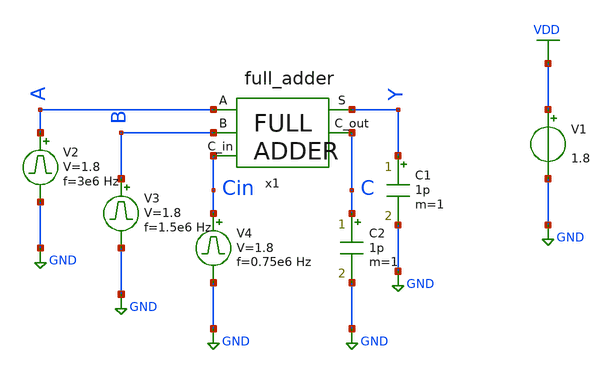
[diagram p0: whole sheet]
** sch_path: library/xschem/full_adder_tb.sch
**.subckt full_adder_tb
V1 VDD GND 1.8
V2 A GND pulse 0 1.8 '0.495/ 3e6 ' '0.01/3e6 ' '0.01/3e6 ' '0.49/3e6 ' '1/3e6 '
C1 Y GND 1p m=1
V3 B GND pulse 0 1.8 '0.495/ 1.5e6 ' '0.01/1.5e6 ' '0.01/1.5e6 ' '0.49/1.5e6 ' '1/1.5e6 '
x1 A B Y Cin C full_adder
C2 C GND 1p m=1
V4 Cin GND pulse 0 1.8 '0.495/ 0.75e6 ' '0.01/0.75e6 ' '0.01/0.75e6 ' '0.49/0.75e6 ' '1/0.75e6 '
**** begin user architecture code


.control
save all
tran 1n 2u
plot V(Y) V(C)+2 V(A)+4 V(B)+6 V(Cin)+8
.endc


** opencircuitdesign pdks install
.lib $::SKYWATER_MODELS/sky130.lib.spice tt


**** end user architecture code
**.ends

* expanding   symbol:  full_adder.sym # of pins=5
** sym_path: library/xschem/full_adder.sym
** sch_path: library/xschem/full_adder.sch
.subckt full_adder A B S C_in C_out
*.opin S
*.ipin A
*.ipin B
*.opin C_out
*.ipin C_in
x9 net2 net3 net1 nor2
x10 net1 C_out inv
x1 A net4 B net2 half_adder
x2 net4 S C_in net3 half_adder
.ends


* expanding   symbol:  nor2.sym # of pins=3
** sym_path: library/xschem/nor2.sym
** sch_path: library/xschem/nor2.sch
.subckt nor2 A B Y
*.opin Y
*.ipin A
*.ipin B
XM1 Y B GND GND sky130_fd_pr__nfet_01v8 L=0.15 W=1 nf=1 ad='int((nf+1)/2) * W/nf * 0.29' as='int((nf+2)/2) * W/nf * 0.29'
+ pd='2*int((nf+1)/2) * (W/nf + 0.29)' ps='2*int((nf+2)/2) * (W/nf + 0.29)' nrd='0.29 / W' nrs='0.29 / W'
+ sa=0 sb=0 sd=0 mult=1 m=1
XM2 Y B net1 VDD sky130_fd_pr__pfet_01v8 L=0.15 W=1 nf=1 ad='int((nf+1)/2) * W/nf * 0.29' as='int((nf+2)/2) * W/nf * 0.29'
+ pd='2*int((nf+1)/2) * (W/nf + 0.29)' ps='2*int((nf+2)/2) * (W/nf + 0.29)' nrd='0.29 / W' nrs='0.29 / W'
+ sa=0 sb=0 sd=0 mult=1 m=1
XM3 net1 A VDD VDD sky130_fd_pr__pfet_01v8 L=0.15 W=1 nf=1 ad='int((nf+1)/2) * W/nf * 0.29' as='int((nf+2)/2) * W/nf * 0.29'
+ pd='2*int((nf+1)/2) * (W/nf + 0.29)' ps='2*int((nf+2)/2) * (W/nf + 0.29)' nrd='0.29 / W' nrs='0.29 / W'
+ sa=0 sb=0 sd=0 mult=1 m=1
XM4 Y A GND GND sky130_fd_pr__nfet_01v8 L=0.15 W=1 nf=1 ad='int((nf+1)/2) * W/nf * 0.29' as='int((nf+2)/2) * W/nf * 0.29'
+ pd='2*int((nf+1)/2) * (W/nf + 0.29)' ps='2*int((nf+2)/2) * (W/nf + 0.29)' nrd='0.29 / W' nrs='0.29 / W'
+ sa=0 sb=0 sd=0 mult=1 m=1
.ends


* expanding   symbol:  inv.sym # of pins=2
** sym_path: library/xschem/inv.sym
** sch_path: library/xschem/inv.sch
.subckt inv A Y
*.opin Y
*.ipin A
XM1 Y A GND GND sky130_fd_pr__nfet_01v8 L=0.15 W=1 nf=1 ad='int((nf+1)/2) * W/nf * 0.29' as='int((nf+2)/2) * W/nf * 0.29'
+ pd='2*int((nf+1)/2) * (W/nf + 0.29)' ps='2*int((nf+2)/2) * (W/nf + 0.29)' nrd='0.29 / W' nrs='0.29 / W'
+ sa=0 sb=0 sd=0 mult=1 m=1
XM2 Y A VDD VDD sky130_fd_pr__pfet_01v8 L=0.15 W=1 nf=1 ad='int((nf+1)/2) * W/nf * 0.29' as='int((nf+2)/2) * W/nf * 0.29'
+ pd='2*int((nf+1)/2) * (W/nf + 0.29)' ps='2*int((nf+2)/2) * (W/nf + 0.29)' nrd='0.29 / W' nrs='0.29 / W'
+ sa=0 sb=0 sd=0 mult=1 m=1
.ends


* expanding   symbol:  half_adder.sym # of pins=4
** sym_path: library/xschem/half_adder.sym
** sch_path: library/xschem/half_adder.sch
.subckt half_adder A S B C_out
*.opin S
*.ipin A
*.ipin B
*.opin C_out
x2 A B net1 net2 S xor2
x3 A net1 inv
x4 B net2 inv
x1 A net3 B nand2
x8 net3 C_out inv
.ends


* expanding   symbol:  xor2.sym # of pins=5
** sym_path: library/xschem/xor2.sym
** sch_path: library/xschem/xor2.sch
.subckt xor2 A B NOT_A NOT_B Y
*.opin Y
*.ipin A
*.ipin B
*.ipin NOT_A
*.ipin NOT_B
XM1 Y NOT_B net2 GND sky130_fd_pr__nfet_01v8 L=0.15 W=1 nf=1 ad='int((nf+1)/2) * W/nf * 0.29' as='int((nf+2)/2) * W/nf * 0.29'
+ pd='2*int((nf+1)/2) * (W/nf + 0.29)' ps='2*int((nf+2)/2) * (W/nf + 0.29)' nrd='0.29 / W' nrs='0.29 / W'
+ sa=0 sb=0 sd=0 mult=1 m=1
XM2 net1 A VDD VDD sky130_fd_pr__pfet_01v8 L=0.15 W=1 nf=1 ad='int((nf+1)/2) * W/nf * 0.29' as='int((nf+2)/2) * W/nf * 0.29'
+ pd='2*int((nf+1)/2) * (W/nf + 0.29)' ps='2*int((nf+2)/2) * (W/nf + 0.29)' nrd='0.29 / W' nrs='0.29 / W'
+ sa=0 sb=0 sd=0 mult=1 m=1
XM4 net2 NOT_A GND GND sky130_fd_pr__nfet_01v8 L=0.15 W=1 nf=1 ad='int((nf+1)/2) * W/nf * 0.29' as='int((nf+2)/2) * W/nf * 0.29'
+ pd='2*int((nf+1)/2) * (W/nf + 0.29)' ps='2*int((nf+2)/2) * (W/nf + 0.29)' nrd='0.29 / W' nrs='0.29 / W'
+ sa=0 sb=0 sd=0 mult=1 m=1
XM3 net1 B VDD VDD sky130_fd_pr__pfet_01v8 L=0.15 W=1 nf=1 ad='int((nf+1)/2) * W/nf * 0.29' as='int((nf+2)/2) * W/nf * 0.29'
+ pd='2*int((nf+1)/2) * (W/nf + 0.29)' ps='2*int((nf+2)/2) * (W/nf + 0.29)' nrd='0.29 / W' nrs='0.29 / W'
+ sa=0 sb=0 sd=0 mult=1 m=1
XM5 Y NOT_B net1 VDD sky130_fd_pr__pfet_01v8 L=0.15 W=1 nf=1 ad='int((nf+1)/2) * W/nf * 0.29' as='int((nf+2)/2) * W/nf * 0.29'
+ pd='2*int((nf+1)/2) * (W/nf + 0.29)' ps='2*int((nf+2)/2) * (W/nf + 0.29)' nrd='0.29 / W' nrs='0.29 / W'
+ sa=0 sb=0 sd=0 mult=1 m=1
XM6 Y NOT_A net1 VDD sky130_fd_pr__pfet_01v8 L=0.15 W=1 nf=1 ad='int((nf+1)/2) * W/nf * 0.29' as='int((nf+2)/2) * W/nf * 0.29'
+ pd='2*int((nf+1)/2) * (W/nf + 0.29)' ps='2*int((nf+2)/2) * (W/nf + 0.29)' nrd='0.29 / W' nrs='0.29 / W'
+ sa=0 sb=0 sd=0 mult=1 m=1
XM7 Y A net3 GND sky130_fd_pr__nfet_01v8 L=0.15 W=1 nf=1 ad='int((nf+1)/2) * W/nf * 0.29' as='int((nf+2)/2) * W/nf * 0.29'
+ pd='2*int((nf+1)/2) * (W/nf + 0.29)' ps='2*int((nf+2)/2) * (W/nf + 0.29)' nrd='0.29 / W' nrs='0.29 / W'
+ sa=0 sb=0 sd=0 mult=1 m=1
XM8 net3 B GND GND sky130_fd_pr__nfet_01v8 L=0.15 W=1 nf=1 ad='int((nf+1)/2) * W/nf * 0.29' as='int((nf+2)/2) * W/nf * 0.29'
+ pd='2*int((nf+1)/2) * (W/nf + 0.29)' ps='2*int((nf+2)/2) * (W/nf + 0.29)' nrd='0.29 / W' nrs='0.29 / W'
+ sa=0 sb=0 sd=0 mult=1 m=1
.ends


* expanding   symbol:  nand2.sym # of pins=3
** sym_path: library/xschem/nand2.sym
** sch_path: library/xschem/nand2.sch
.subckt nand2 A Y B
*.opin Y
*.ipin A
*.ipin B
XM1 Y B net1 GND sky130_fd_pr__nfet_01v8 L=0.15 W=1 nf=1 ad='int((nf+1)/2) * W/nf * 0.29' as='int((nf+2)/2) * W/nf * 0.29'
+ pd='2*int((nf+1)/2) * (W/nf + 0.29)' ps='2*int((nf+2)/2) * (W/nf + 0.29)' nrd='0.29 / W' nrs='0.29 / W'
+ sa=0 sb=0 sd=0 mult=1 m=1
XM2 Y B VDD VDD sky130_fd_pr__pfet_01v8 L=0.15 W=1 nf=1 ad='int((nf+1)/2) * W/nf * 0.29' as='int((nf+2)/2) * W/nf * 0.29'
+ pd='2*int((nf+1)/2) * (W/nf + 0.29)' ps='2*int((nf+2)/2) * (W/nf + 0.29)' nrd='0.29 / W' nrs='0.29 / W'
+ sa=0 sb=0 sd=0 mult=1 m=1
XM3 Y A VDD VDD sky130_fd_pr__pfet_01v8 L=0.15 W=1 nf=1 ad='int((nf+1)/2) * W/nf * 0.29' as='int((nf+2)/2) * W/nf * 0.29'
+ pd='2*int((nf+1)/2) * (W/nf + 0.29)' ps='2*int((nf+2)/2) * (W/nf + 0.29)' nrd='0.29 / W' nrs='0.29 / W'
+ sa=0 sb=0 sd=0 mult=1 m=1
XM4 net1 A GND GND sky130_fd_pr__nfet_01v8 L=0.15 W=1 nf=1 ad='int((nf+1)/2) * W/nf * 0.29' as='int((nf+2)/2) * W/nf * 0.29'
+ pd='2*int((nf+1)/2) * (W/nf + 0.29)' ps='2*int((nf+2)/2) * (W/nf + 0.29)' nrd='0.29 / W' nrs='0.29 / W'
+ sa=0 sb=0 sd=0 mult=1 m=1
.ends

.GLOBAL VDD
.GLOBAL GND
.end
